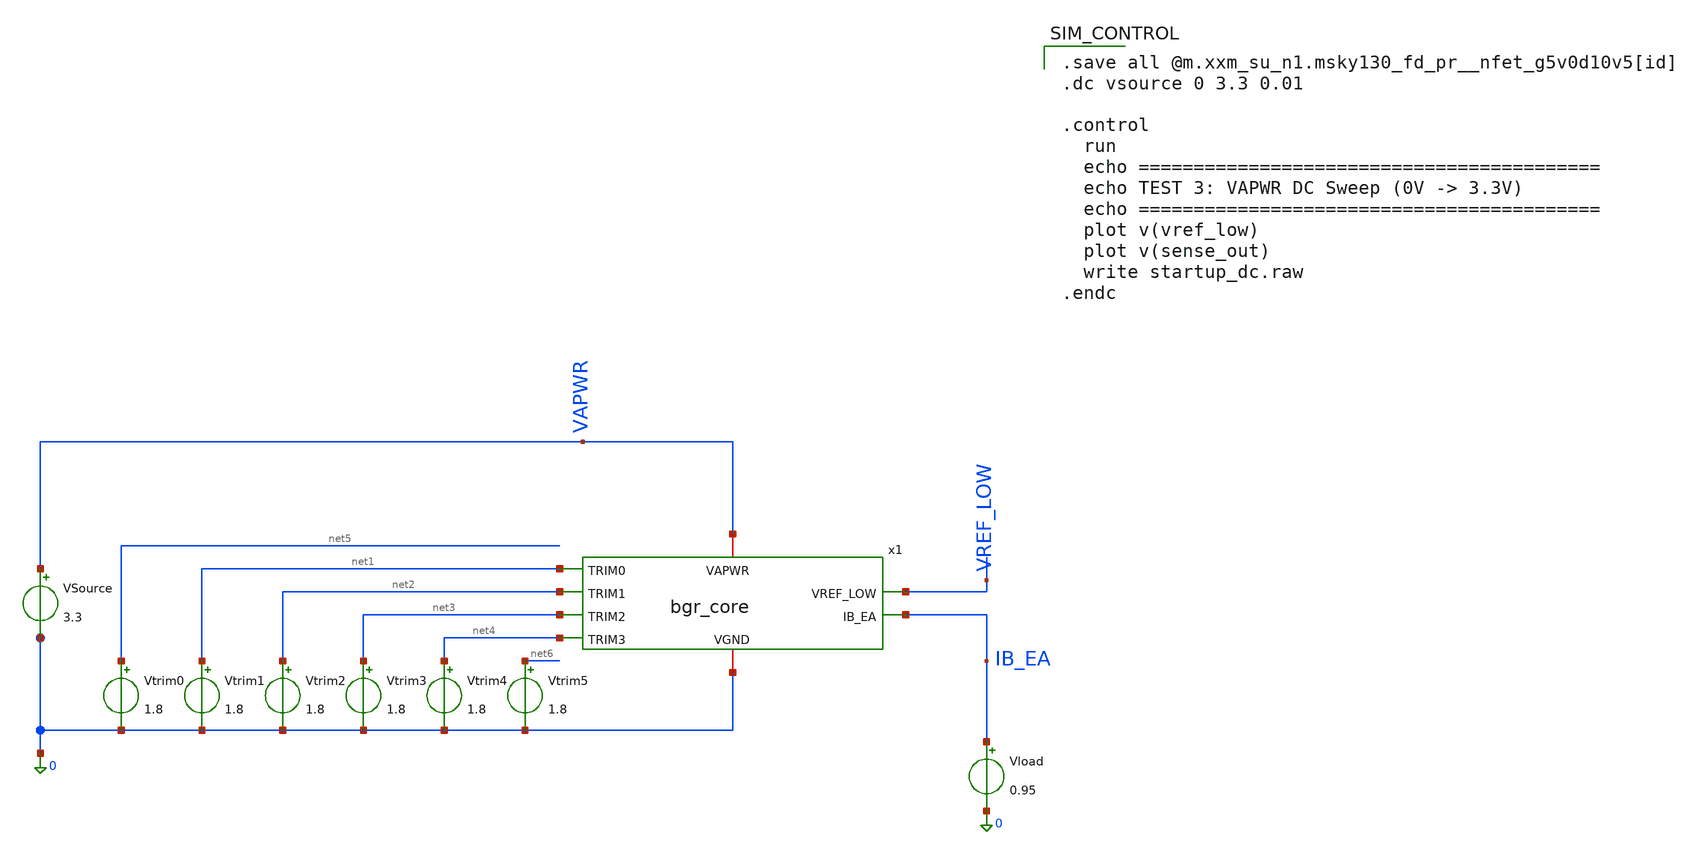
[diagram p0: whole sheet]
** sch_path: designs/bgr_ldo/bgr/bgr_core_tb2.sch
**.subckt bgr_core_tb2
VSource VAPWR 0 3.3
Vload IB_EA 0 0.95
Vtrim0 net5 0 1.8
Vtrim1 net1 0 1.8
Vtrim2 net2 0 1.8
Vtrim3 net3 0 1.8
x1 VAPWR VREF_LOW IB_EA net1 net2 net3 net4 0 bgr_core
Vtrim4 net4 0 1.8
Vtrim5 net6 0 1.8
**** begin user architecture code

.save all @m.xxm_su_n1.msky130_fd_pr__nfet_g5v0d10v5[id]
.dc vsource 0 3.3 0.01

.control
  run
  echo ==========================================
  echo TEST 3: VAPWR DC Sweep (0V -> 3.3V)
  echo ==========================================
  plot v(vref_low)
  plot v(sense_out)
  write startup_dc.raw
.endc


** opencircuitdesign pdks install
.lib $::SKYWATER_MODELS/sky130.lib.spice tt

**** end user architecture code
**.ends
.end
